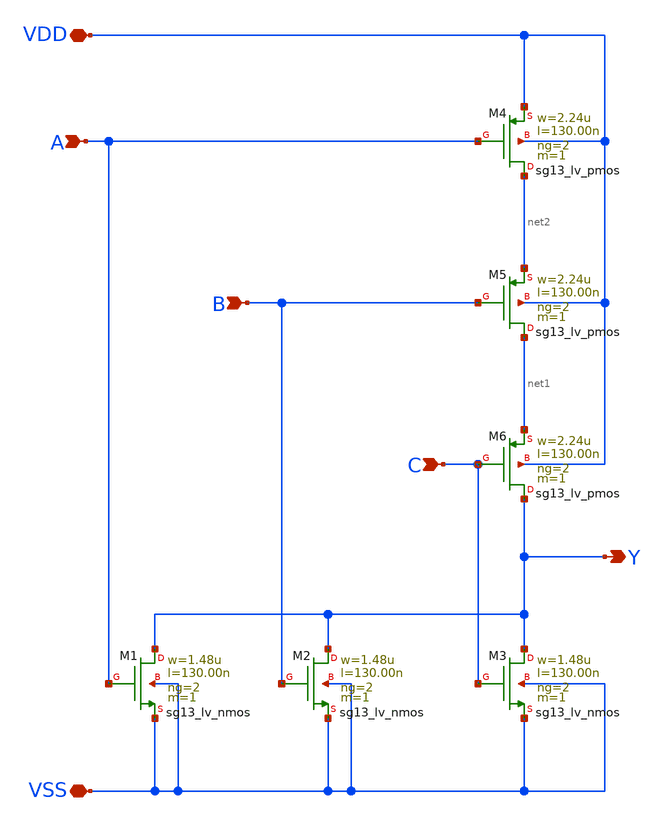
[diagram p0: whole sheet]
** sch_path: ihp-sg13g2/libs.tech/xschem/sg13g2_stdcells/sg13g2_nor3_2.sch
**.subckt sg13g2_nor3_2 B VDD VSS Y A C
*.ipin B
*.iopin VDD
*.iopin VSS
*.opin Y
*.ipin A
*.ipin C
XM1 Y A VSS VSS sg13_lv_nmos w=1.48u l=130.00n ng=2 m=1 mm_ok=1
XM2 Y B VSS VSS sg13_lv_nmos w=1.48u l=130.00n ng=2 m=1 mm_ok=1
XM3 Y C VSS VSS sg13_lv_nmos w=1.48u l=130.00n ng=2 m=1 mm_ok=1
XM4 net2 A VDD VDD sg13_lv_pmos w=2.24u l=130.00n ng=2 m=1 mm_ok=1
XM5 net1 B net2 VDD sg13_lv_pmos w=2.24u l=130.00n ng=2 m=1 mm_ok=1
XM6 Y C net1 VDD sg13_lv_pmos w=2.24u l=130.00n ng=2 m=1 mm_ok=1
**.ends
.end
